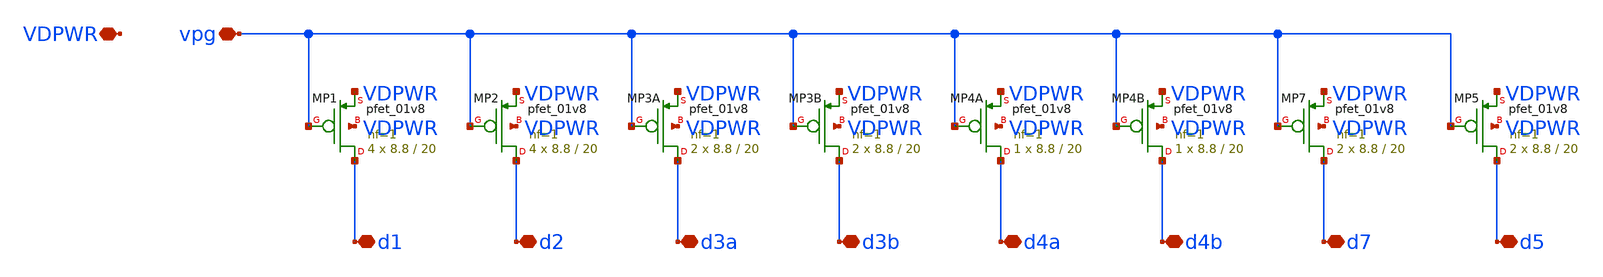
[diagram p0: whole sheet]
** sch_path: xschem/bg_mirror.sch
**.subckt bg_mirror vpg VDPWR d1 d2 d3a d3b d4a d4b d7 d5
*.iopin vpg
*.iopin VDPWR
*.iopin d1
*.iopin d2
*.iopin d3a
*.iopin d3b
*.iopin d4a
*.iopin d4b
*.iopin d7
*.iopin d5
XMP1 d1 vpg VDPWR VDPWR sky130_fd_pr__pfet_01v8 L=20 W=8.8 nf=1 ad='int((1 + 1)/2) * 8.8 / 1 * 0.29'
+ as='int((1 + 2)/2) * 8.8 / 1 * 0.29' pd='2*int((1 + 1)/2) * (8.8 / 1 + 0.29)' ps='2*int((1 + 2)/2) * (8.8 / 1 + 0.29)'
+ nrd='0.29 / 8.8 ' nrs='0.29 / 8.8 ' sa=0 sb=0 sd=0 mult=4 m=4
XMP2 d2 vpg VDPWR VDPWR sky130_fd_pr__pfet_01v8 L=20 W=8.8 nf=1 ad='int((1 + 1)/2) * 8.8 / 1 * 0.29'
+ as='int((1 + 2)/2) * 8.8 / 1 * 0.29' pd='2*int((1 + 1)/2) * (8.8 / 1 + 0.29)' ps='2*int((1 + 2)/2) * (8.8 / 1 + 0.29)'
+ nrd='0.29 / 8.8 ' nrs='0.29 / 8.8 ' sa=0 sb=0 sd=0 mult=4 m=4
XMP3A d3a vpg VDPWR VDPWR sky130_fd_pr__pfet_01v8 L=20 W=8.8 nf=1 ad='int((1 + 1)/2) * 8.8 / 1 * 0.29'
+ as='int((1 + 2)/2) * 8.8 / 1 * 0.29' pd='2*int((1 + 1)/2) * (8.8 / 1 + 0.29)' ps='2*int((1 + 2)/2) * (8.8 / 1 + 0.29)'
+ nrd='0.29 / 8.8 ' nrs='0.29 / 8.8 ' sa=0 sb=0 sd=0 mult=2 m=2
XMP3B d3b vpg VDPWR VDPWR sky130_fd_pr__pfet_01v8 L=20 W=8.8 nf=1 ad='int((1 + 1)/2) * 8.8 / 1 * 0.29'
+ as='int((1 + 2)/2) * 8.8 / 1 * 0.29' pd='2*int((1 + 1)/2) * (8.8 / 1 + 0.29)' ps='2*int((1 + 2)/2) * (8.8 / 1 + 0.29)'
+ nrd='0.29 / 8.8 ' nrs='0.29 / 8.8 ' sa=0 sb=0 sd=0 mult=2 m=2
XMP4A d4a vpg VDPWR VDPWR sky130_fd_pr__pfet_01v8 L=20 W=8.8 nf=1 ad='int((1 + 1)/2) * 8.8 / 1 * 0.29'
+ as='int((1 + 2)/2) * 8.8 / 1 * 0.29' pd='2*int((1 + 1)/2) * (8.8 / 1 + 0.29)' ps='2*int((1 + 2)/2) * (8.8 / 1 + 0.29)'
+ nrd='0.29 / 8.8 ' nrs='0.29 / 8.8 ' sa=0 sb=0 sd=0 mult=1 m=1
XMP4B d4b vpg VDPWR VDPWR sky130_fd_pr__pfet_01v8 L=20 W=8.8 nf=1 ad='int((1 + 1)/2) * 8.8 / 1 * 0.29'
+ as='int((1 + 2)/2) * 8.8 / 1 * 0.29' pd='2*int((1 + 1)/2) * (8.8 / 1 + 0.29)' ps='2*int((1 + 2)/2) * (8.8 / 1 + 0.29)'
+ nrd='0.29 / 8.8 ' nrs='0.29 / 8.8 ' sa=0 sb=0 sd=0 mult=1 m=1
XMP7 d7 vpg VDPWR VDPWR sky130_fd_pr__pfet_01v8 L=20 W=8.8 nf=1 ad='int((1 + 1)/2) * 8.8 / 1 * 0.29'
+ as='int((1 + 2)/2) * 8.8 / 1 * 0.29' pd='2*int((1 + 1)/2) * (8.8 / 1 + 0.29)' ps='2*int((1 + 2)/2) * (8.8 / 1 + 0.29)'
+ nrd='0.29 / 8.8 ' nrs='0.29 / 8.8 ' sa=0 sb=0 sd=0 mult=2 m=2
XMP5 d5 vpg VDPWR VDPWR sky130_fd_pr__pfet_01v8 L=20 W=8.8 nf=1 ad='int((1 + 1)/2) * 8.8 / 1 * 0.29'
+ as='int((1 + 2)/2) * 8.8 / 1 * 0.29' pd='2*int((1 + 1)/2) * (8.8 / 1 + 0.29)' ps='2*int((1 + 2)/2) * (8.8 / 1 + 0.29)'
+ nrd='0.29 / 8.8 ' nrs='0.29 / 8.8 ' sa=0 sb=0 sd=0 mult=2 m=2
**.ends
.end
